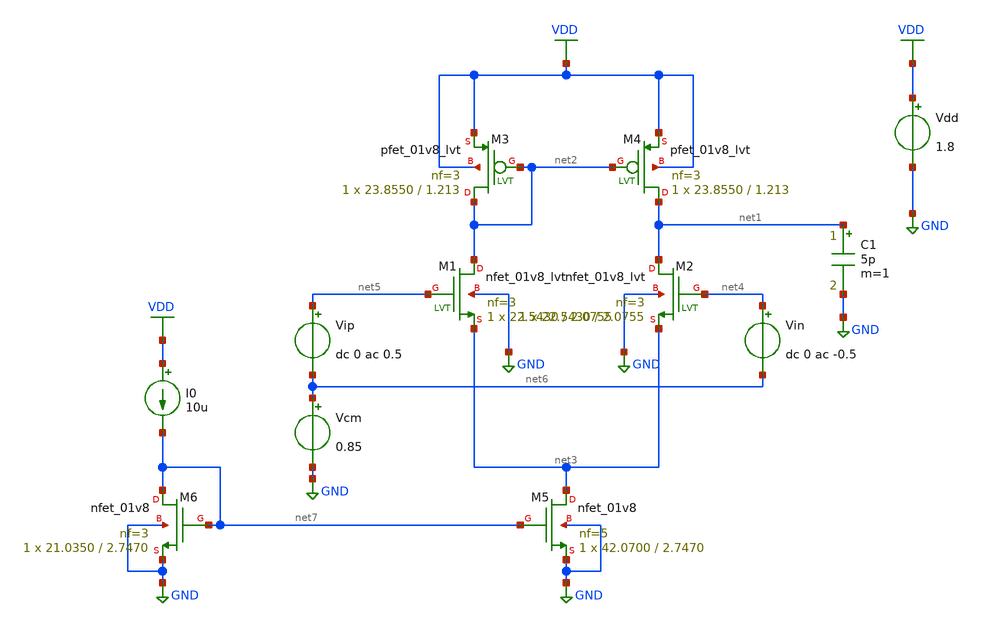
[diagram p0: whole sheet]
** sch_path: part2-full-spec-icmr-cmrr/cir/part2_OTA_advacned.sch
**.subckt part2_OTA_advacned
XM5 net3 net7 GND GND sky130_fd_pr__nfet_01v8 L=2.7470 W=42.0700 nf=5 ad='int((5 + 1)/2) * 42.0700 / 5 * 0.29'
+ as='int((5 + 2)/2) * 42.0700 / 5 * 0.29' pd='2*int((5 + 1)/2) * (42.0700 / 5 + 0.29)' ps='2*int((5 + 2)/2) * (42.0700 / 5 + 0.29)'
+ nrd='0.29 / 42.0700 ' nrs='0.29 / 42.0700 ' sa=0 sb=0 sd=0 mult=1 m=1
Vdd VDD GND 1.8
Vcm net6 GND 0.85
Vip net5 net6 dc 0 ac 0.5
Vin net4 net6 dc 0 ac -0.5
C1 net1 GND 5p m=1
XM4 net1 net2 VDD VDD sky130_fd_pr__pfet_01v8_lvt L=1.213 W=23.8550 nf=3 ad='int((3 + 1)/2) * 23.8550 / 3 * 0.29'
+ as='int((3 + 2)/2) * 23.8550 / 3 * 0.29' pd='2*int((3 + 1)/2) * (23.8550 / 3 + 0.29)' ps='2*int((3 + 2)/2) * (23.8550 / 3 + 0.29)'
+ nrd='0.29 / 23.8550 ' nrs='0.29 / 23.8550 ' sa=0 sb=0 sd=0 mult=1 m=1
XM3 net2 net2 VDD VDD sky130_fd_pr__pfet_01v8_lvt L=1.213 W=23.8550 nf=3 ad='int((3 + 1)/2) * 23.8550 / 3 * 0.29'
+ as='int((3 + 2)/2) * 23.8550 / 3 * 0.29' pd='2*int((3 + 1)/2) * (23.8550 / 3 + 0.29)' ps='2*int((3 + 2)/2) * (23.8550 / 3 + 0.29)'
+ nrd='0.29 / 23.8550 ' nrs='0.29 / 23.8550 ' sa=0 sb=0 sd=0 mult=1 m=1
XM6 net7 net7 GND GND sky130_fd_pr__nfet_01v8 L=2.7470 W=21.0350 nf=3 ad='int((3 + 1)/2) * 21.0350 / 3 * 0.29'
+ as='int((3 + 2)/2) * 21.0350 / 3 * 0.29' pd='2*int((3 + 1)/2) * (21.0350 / 3 + 0.29)' ps='2*int((3 + 2)/2) * (21.0350 / 3 + 0.29)'
+ nrd='0.29 / 21.0350 ' nrs='0.29 / 21.0350 ' sa=0 sb=0 sd=0 mult=1 m=1
I0 VDD net7 10u
XM1 net2 net5 net3 GND sky130_fd_pr__nfet_01v8_lvt L=2.0755 W=22.5430 nf=3 ad='int((3 + 1)/2) * 22.5430 / 3 * 0.29'
+ as='int((3 + 2)/2) * 22.5430 / 3 * 0.29' pd='2*int((3 + 1)/2) * (22.5430 / 3 + 0.29)' ps='2*int((3 + 2)/2) * (22.5430 / 3 + 0.29)'
+ nrd='0.29 / 22.5430 ' nrs='0.29 / 22.5430 ' sa=0 sb=0 sd=0 mult=1 m=1
XM2 net1 net4 net3 GND sky130_fd_pr__nfet_01v8_lvt L=2.0755 W=22.5430 nf=3 ad='int((3 + 1)/2) * 22.5430 / 3 * 0.29'
+ as='int((3 + 2)/2) * 22.5430 / 3 * 0.29' pd='2*int((3 + 1)/2) * (22.5430 / 3 + 0.29)' ps='2*int((3 + 2)/2) * (22.5430 / 3 + 0.29)'
+ nrd='0.29 / 22.5430 ' nrs='0.29 / 22.5430 ' sa=0 sb=0 sd=0 mult=1 m=1
**** begin user architecture code


.lib /foss/pdks/sky130A/libs.tech/ngspice/sky130.lib.spice tt


* - Print the oprating points
.op

.control
	save @m.xm1.msky130_fd_pr__nfet_01v8_lvt[gm]
	save @m.xm1.msky130_fd_pr__nfet_01v8_lvt[id]
	save @m.xm1.msky130_fd_pr__nfet_01v8_lvt[gds]

	save @m.xm2.msky130_fd_pr__nfet_01v8_lvt[gm]
	save @m.xm2.msky130_fd_pr__nfet_01v8_lvt[id]
	save @m.xm2.msky130_fd_pr__nfet_01v8_lvt[gds]

	save @m.xm3.msky130_fd_pr__pfet_01v8_lvt[gm]
	save @m.xm3.msky130_fd_pr__pfet_01v8_lvt[id]
	save @m.xm3.msky130_fd_pr__pfet_01v8_lvt[gds]

	save @m.xm4.msky130_fd_pr__pfet_01v8_lvt[gm]
	save @m.xm4.msky130_fd_pr__pfet_01v8_lvt[id]
	save @m.xm4.msky130_fd_pr__pfet_01v8_lvt[gds]

	save @m.xm5.msky130_fd_pr__nfet_01v8[gm]
	save @m.xm5.msky130_fd_pr__nfet_01v8[id]
	save @m.xm5.msky130_fd_pr__nfet_01v8[gds]

	save @m.xm5.msky130_fd_pr__nfet_01v8[gm]
	save @m.xm5.msky130_fd_pr__nfet_01v8[id]
	save @m.xm5.msky130_fd_pr__nfet_01v8[gds]


	save all

	run

	show xm1.msky130_fd_pr__nfet_01v8
	show xm2.msky130_fd_pr__nfet_01v8
	show xm3.msky130_fd_pr__pfet_01v8_lvt
	show xm4.msky130_fd_pr__pfet_01v8_lvt
	show xm5.msky130_fd_pr__nfet_01v8
	show xm6.msky130_fd_pr__nfet_01v8
	show all


.endc




.lib /foss/pdks/sky130A/libs.tech/ngspice/sky130.lib.spice tt



.control

	save all

	ac dec 20 1 100e6

	meas ac dc_gain MAX vdb(net1) from=1 to=10
	let target_gain = dc_gain -3
	meas ac f_3db WHEN vdb(net1) = target_gain
	meas ac gbw WHEN vdb(net1) = 0

	let Av = vdb(net1)

	plot Av title 'DC Gain (Magnitude)'
	plot cph(net1)*180/pi title 'DC Gain (Phase)'

.endc




.lib /foss/pdks/sky130A/libs.tech/ngspice/sky130.lib.spice tt


* - Sweep Vcm and find the optimal operating point (gm, gds, id, biasing, etc)
.dc Vcm 0 1.8 0.1


.control
	save @m.xm1.msky130_fd_pr__nfet_01v8_lvt[gm]
	save @m.xm1.msky130_fd_pr__nfet_01v8_lvt[id]
	save @m.xm1.msky130_fd_pr__nfet_01v8_lvt[gds]

	save @m.xm2.msky130_fd_pr__nfet_01v8_lvt[gm]
	save @m.xm2.msky130_fd_pr__nfet_01v8_lvt[id]
	save @m.xm2.msky130_fd_pr__nfet_01v8_lvt[gds]

	save @m.xm3.msky130_fd_pr__pfet_01v8_lvt[gm]
	save @m.xm3.msky130_fd_pr__pfet_01v8_lvt[id]
	save @m.xm3.msky130_fd_pr__pfet_01v8_lvt[gds]

	save @m.xm4.msky130_fd_pr__pfet_01v8_lvt[gm]
	save @m.xm4.msky130_fd_pr__pfet_01v8_lvt[id]
	save @m.xm4.msky130_fd_pr__pfet_01v8_lvt[gds]

	save @m.xm5.msky130_fd_pr__nfet_01v8[gm]
	save @m.xm5.msky130_fd_pr__nfet_01v8[id]
	save @m.xm5.msky130_fd_pr__nfet_01v8[gds]

	save @m.xm5.msky130_fd_pr__nfet_01v8[gm]
	save @m.xm5.msky130_fd_pr__nfet_01v8[id]
	save @m.xm5.msky130_fd_pr__nfet_01v8[gds]

	save all

	run

	let gm_1_2 = @m.xm1.msky130_fd_pr__nfet_01v8_lvt[gm]
	let i5 = @m.xm5.msky130_fd_pr__nfet_01v8[id]

	plot gm_1_2 title 'VCM vs gm_12'
	plot i5 title 'VCM vs ISS'
	* - Plot VDS3,4 (mirror loads)
	plot v(vdd)-v(net2)  title 'VCM vs vds_34'
	* - Plot VDS1,2 (input pairs)
	plot v(net2)-v(net3) title 'VCM vs vds_12'
	* - Plot VDS5 (tail)
	plot v(net3) title 'VCM vs gvds_5'

.endc




.lib /foss/pdks/sky130A/libs.tech/ngspice/sky130.lib.spice tt



.control

	save all

	* Get Differential Gain
	alter vip ac = 0.5
	alter vin ac = -0.5
	ac dec 20 1 100e6
	let adm_db = vdb(net1)
	plot net1
	plot adm_db

	* Get Common Mode Gain
	alter vip ac = 1.0
	alter vin ac = 1.0
	ac dec 20 1 100e6
	plot net1
	let acm_db = vdb(net1)

	let cmrr_db = ac1.adm_db - ac2.acm_db

	meas ac cmrr_db_val MAX cmrr_db from=1 to=10

	plot acm_db title 'Frequency vs Av_CM'
	plot  cmrr_db title 'Frequency vs CMRR'
.endc


**** end user architecture code
**.ends
.GLOBAL GND
.GLOBAL VDD
.end
